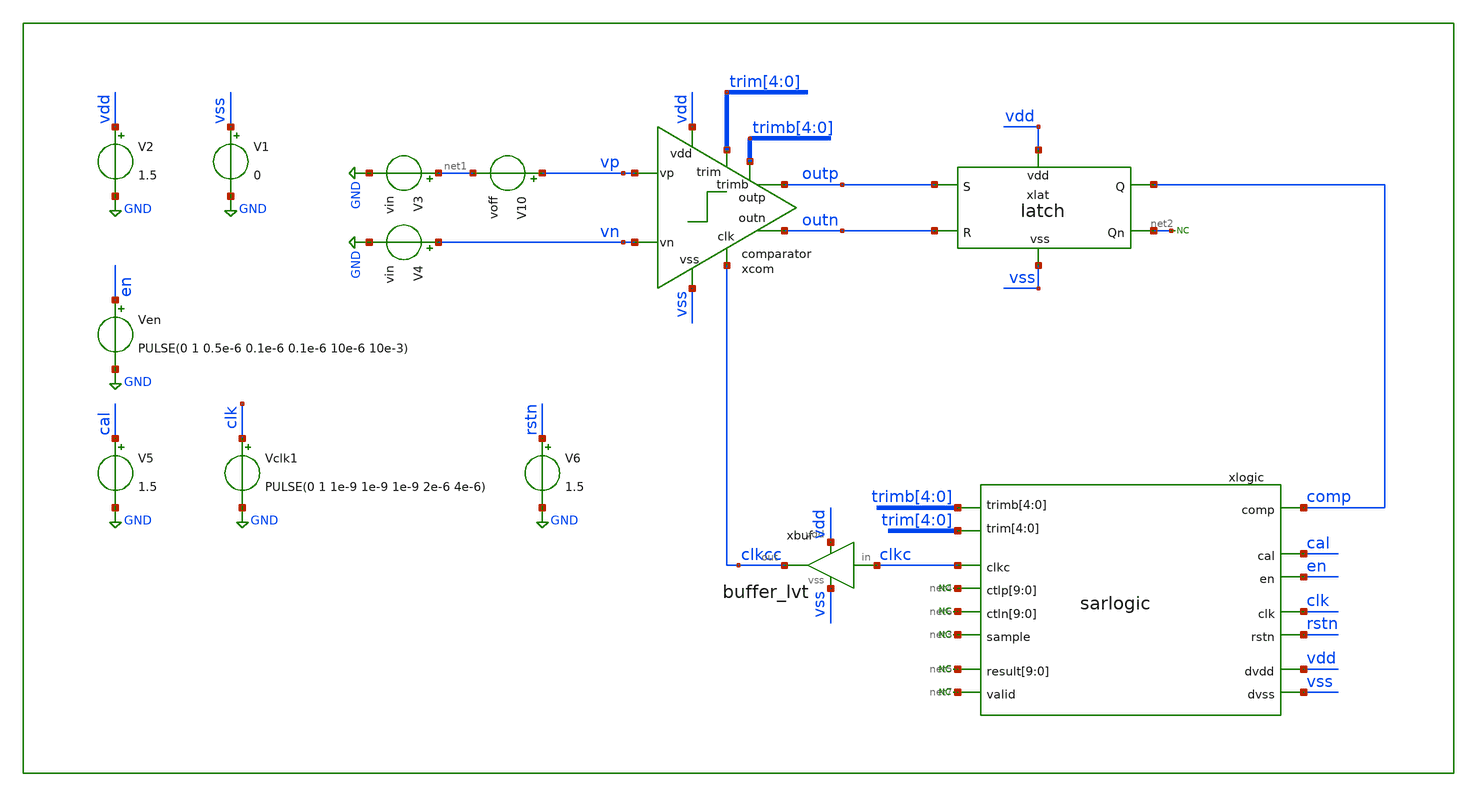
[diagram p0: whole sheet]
** sch_path: xschem/tb/comparator/tran_comparator_trim.sch
**.subckt tran_comparator_trim
xcom vss vdd clkcc outp vp outn vn trim[4] trim[3] trim[2] trim[1] trim[0] trimb[4] trimb[3]
+ trimb[2] trimb[1] trimb[0] comparator
V1 vss GND 0
V2 vdd GND 1.5
V3 net1 GND vin
V4 vn GND vin
V10 vp net1 voff
* noconn #net3
* noconn #net4
xlat vdd comp net2 vss outn outp latch
* noconn #net2
Vclk1 clk GND PULSE(0 1 1e-9 1e-9 1e-9 2e-6 4e-6)
V5 cal GND 1.5
Ven en GND PULSE(0 1 0.5e-6 0.1e-6 0.1e-6 10e-6 10e-3)
V6 rstn GND 1.5
xlogic trim[4] trim[3] trim[2] trim[1] trim[0] trimb[4] trimb[3] trimb[2] trimb[1] trimb[0] clkc
+ comp cal en net4[9] net4[8] net4[7] net4[6] net4[5] net4[4] net4[3] net4[2] net4[1] net4[0] clk net5[9]
+ net5[8] net5[7] net5[6] net5[5] net5[4] net5[3] net5[2] net5[1] net5[0] net6[9] net6[8] net6[7] net6[6]
+ net6[5] net6[4] net6[3] net6[2] net6[1] net6[0] net7 rstn net3 vdd vss sarlogic
* noconn #net6
* noconn #net5
* noconn #net7
xbuf vdd clkc clkcc vss buffer_lvt
**** begin user architecture code
 .include $::DESIGN_PATH/sar_10b/control/cmos_cells_digital.sp
.include $::DESIGN_PATH/sar_10b/control/sarlogic.sp

.param MC_SWITCH=0
.param vin=0.75
.param voff=0

.options method trap

.control
tran 100e-9 200e-6

meas tran tip_a WHEN v(xcom.ip)=1 fall=2
meas tran tin_a WHEN v(xcom.in)=1 fall=2
meas tran tip_b WHEN v(xcom.ip)=1 fall=-2
meas tran tin_b WHEN v(xcom.in)=1 fall=-2

let delta_a = abs(tip_a-tin_a)
let delta_b = abs(tip_b-tin_b)

print delta_a
print delta_b

.endc


* FET CORNERS
.include $::SKYWATER_MODELS/corners/tt.spice
*.include $::SKYWATER_MODELS/corners/ff.spice
*.include $::SKYWATER_MODELS/corners/ss.spice
*.include $::SKYWATER_MODELS/corners/sf.spice
*.include $::SKYWATER_MODELS/corners/fs.spice

* TT + R + C
*.include $::SKYWATER_MODELS/corners/tt_rmax_cmax.spice
*.include $::SKYWATER_MODELS/corners/tt_rmin_cmin.spice
*.include $::SKYWATER_MODELS/corners/tt_rmax_cmin.spice
*.include $::SKYWATER_MODELS/corners/tt_rmin_cmax.spice

* FF + R + C
*.include $::SKYWATER_MODELS/corners/ff_rmax_cmax.spice
*.include $::SKYWATER_MODELS/corners/ff_rmin_cmin.spice
*.include $::SKYWATER_MODELS/corners/ff_rmax_cmin.spice
*.include $::SKYWATER_MODELS/corners/ff_rmin_cmax.spice


* SS + R + C
*.include $::SKYWATER_MODELS/corners/ss_rmax_cmax.spice
*.include $::SKYWATER_MODELS/corners/ss_rmin_cmin.spice
*.include $::SKYWATER_MODELS/corners/ss_rmax_cmin.spice
*.include $::SKYWATER_MODELS/corners/ss_rmin_cmax.spice

* SF + R + C
*.include $::SKYWATER_MODELS/corners/sf_rmax_cmax.spice
*.include $::SKYWATER_MODELS/corners/sf_rmin_cmin.spice
*.include $::SKYWATER_MODELS/corners/sf_rmax_cmin.spice
*.include $::SKYWATER_MODELS/corners/sf_rmin_cmax.spice

* FS + R + C
*.include $::SKYWATER_MODELS/corners/fs_rmax_cmax.spice
*.include $::SKYWATER_MODELS/corners/fs_rmin_cmin.spice
*.include $::SKYWATER_MODELS/corners/fs_rmax_cmin.spice
*.include $::SKYWATER_MODELS/corners/fs_rmin_cmax.spice

**** end user architecture code
**.ends

* expanding   symbol:  sar_10b/comparator/comparator.sym # of pins=9
** sym_path: xschem/sar_10b/comparator/comparator.sym
** sch_path: xschem/sar_10b/comparator/comparator.sch
.subckt comparator vss vdd clk outp vp outn vn trim[4] trim[3] trim[2] trim[1] trim[0] trimb[4]
+ trimb[3] trimb[2] trimb[1] trimb[0]
*.ipin vn
*.ipin vp
*.ipin clk
*.iopin vdd
*.iopin vss
*.opin outp
*.opin outn
*.ipin trim[4],trim[3],trim[2],trim[1],trim[0]
*.ipin trimb[4],trimb[3],trimb[2],trimb[1],trimb[0]
XMdiff diff clk vss vss sky130_fd_pr__nfet_01v8 L=0.3 W=1 nf=1 ad='int((nf+1)/2) * W/nf * 0.29' as='int((nf+2)/2) * W/nf * 0.29'
+ pd='2*int((nf+1)/2) * (W/nf + 0.29)' ps='2*int((nf+2)/2) * (W/nf + 0.29)' nrd='0.29 / W' nrs='0.29 / W'
+ sa=0 sb=0 sd=0 mult=2 m=2
XMinn in vn diff vss sky130_fd_pr__nfet_01v8 L=0.3 W=1 nf=1 ad='int((nf+1)/2) * W/nf * 0.29' as='int((nf+2)/2) * W/nf * 0.29'
+ pd='2*int((nf+1)/2) * (W/nf + 0.29)' ps='2*int((nf+2)/2) * (W/nf + 0.29)' nrd='0.29 / W' nrs='0.29 / W'
+ sa=0 sb=0 sd=0 mult=1 m=1
XMinp ip vp diff vss sky130_fd_pr__nfet_01v8 L=0.3 W=1 nf=1 ad='int((nf+1)/2) * W/nf * 0.29' as='int((nf+2)/2) * W/nf * 0.29'
+ pd='2*int((nf+1)/2) * (W/nf + 0.29)' ps='2*int((nf+2)/2) * (W/nf + 0.29)' nrd='0.29 / W' nrs='0.29 / W'
+ sa=0 sb=0 sd=0 mult=1 m=1
XMl4 outp outn vdd vdd sky130_fd_pr__pfet_01v8 L=0.3 W=1 nf=1 ad='int((nf+1)/2) * W/nf * 0.29' as='int((nf+2)/2) * W/nf * 0.29'
+ pd='2*int((nf+1)/2) * (W/nf + 0.29)' ps='2*int((nf+2)/2) * (W/nf + 0.29)' nrd='0.29 / W' nrs='0.29 / W'
+ sa=0 sb=0 sd=0 mult=1 m=1
XMl3 outn outp vdd vdd sky130_fd_pr__pfet_01v8 L=0.3 W=1 nf=1 ad='int((nf+1)/2) * W/nf * 0.29' as='int((nf+2)/2) * W/nf * 0.29'
+ pd='2*int((nf+1)/2) * (W/nf + 0.29)' ps='2*int((nf+2)/2) * (W/nf + 0.29)' nrd='0.29 / W' nrs='0.29 / W'
+ sa=0 sb=0 sd=0 mult=1 m=1
XM3 outp clk vdd vdd sky130_fd_pr__pfet_01v8 L=0.3 W=1 nf=1 ad='int((nf+1)/2) * W/nf * 0.29' as='int((nf+2)/2) * W/nf * 0.29'
+ pd='2*int((nf+1)/2) * (W/nf + 0.29)' ps='2*int((nf+2)/2) * (W/nf + 0.29)' nrd='0.29 / W' nrs='0.29 / W'
+ sa=0 sb=0 sd=0 mult=1 m=1
XM2 outn clk vdd vdd sky130_fd_pr__pfet_01v8 L=0.3 W=1 nf=1 ad='int((nf+1)/2) * W/nf * 0.29' as='int((nf+2)/2) * W/nf * 0.29'
+ pd='2*int((nf+1)/2) * (W/nf + 0.29)' ps='2*int((nf+2)/2) * (W/nf + 0.29)' nrd='0.29 / W' nrs='0.29 / W'
+ sa=0 sb=0 sd=0 mult=1 m=1
XMl1 outn outp in vss sky130_fd_pr__nfet_01v8 L=0.3 W=1 nf=1 ad='int((nf+1)/2) * W/nf * 0.29' as='int((nf+2)/2) * W/nf * 0.29'
+ pd='2*int((nf+1)/2) * (W/nf + 0.29)' ps='2*int((nf+2)/2) * (W/nf + 0.29)' nrd='0.29 / W' nrs='0.29 / W'
+ sa=0 sb=0 sd=0 mult=1 m=1
XMl2 outp outn ip vss sky130_fd_pr__nfet_01v8 L=0.3 W=1 nf=1 ad='int((nf+1)/2) * W/nf * 0.29' as='int((nf+2)/2) * W/nf * 0.29'
+ pd='2*int((nf+1)/2) * (W/nf + 0.29)' ps='2*int((nf+2)/2) * (W/nf + 0.29)' nrd='0.29 / W' nrs='0.29 / W'
+ sa=0 sb=0 sd=0 mult=1 m=1
XM4 ip clk vdd vdd sky130_fd_pr__pfet_01v8 L=0.3 W=1 nf=1 ad='int((nf+1)/2) * W/nf * 0.29' as='int((nf+2)/2) * W/nf * 0.29'
+ pd='2*int((nf+1)/2) * (W/nf + 0.29)' ps='2*int((nf+2)/2) * (W/nf + 0.29)' nrd='0.29 / W' nrs='0.29 / W'
+ sa=0 sb=0 sd=0 mult=1 m=1
XM1 in clk vdd vdd sky130_fd_pr__pfet_01v8 L=0.3 W=1 nf=1 ad='int((nf+1)/2) * W/nf * 0.29' as='int((nf+2)/2) * W/nf * 0.29'
+ pd='2*int((nf+1)/2) * (W/nf + 0.29)' ps='2*int((nf+2)/2) * (W/nf + 0.29)' nrd='0.29 / W' nrs='0.29 / W'
+ sa=0 sb=0 sd=0 mult=1 m=1
x2 in trim[4] trim[3] trim[2] trim[1] trim[0] vss trim
x3 ip trimb[4] trimb[3] trimb[2] trimb[1] trimb[0] vss trim
.ends


* expanding   symbol:  sar_10b/latch/latch.sym # of pins=6
** sym_path: xschem/sar_10b/latch/latch.sym
** sch_path: xschem/sar_10b/latch/latch.sch
.subckt latch vdd Q Qn vss R S
*.ipin S
*.ipin R
*.iopin vss
*.iopin vdd
*.opin Q
*.opin Qn
x1 vdd Qn Q vss inv_lvt
x2 vdd Q Qn vss inv_lvt
x3 vdd R net2 vss inv_lvt
x4 vdd S net1 vss inv_lvt
XM3 Qn net1 vss vss sky130_fd_pr__nfet_01v8_lvt L=0.4 W=1 nf=1 ad='int((nf+1)/2) * W/nf * 0.29' as='int((nf+2)/2) * W/nf * 0.29'
+ pd='2*int((nf+1)/2) * (W/nf + 0.29)' ps='2*int((nf+2)/2) * (W/nf + 0.29)' nrd='0.29 / W' nrs='0.29 / W'
+ sa=0 sb=0 sd=0 mult=1 m=1
XM1 Q net2 vss vss sky130_fd_pr__nfet_01v8_lvt L=0.4 W=1 nf=1 ad='int((nf+1)/2) * W/nf * 0.29' as='int((nf+2)/2) * W/nf * 0.29'
+ pd='2*int((nf+1)/2) * (W/nf + 0.29)' ps='2*int((nf+2)/2) * (W/nf + 0.29)' nrd='0.29 / W' nrs='0.29 / W'
+ sa=0 sb=0 sd=0 mult=1 m=1
.ends


* expanding   symbol:  sar_10b/control/sarlogic.sym # of pins=15
** sym_path: xschem/sar_10b/control/sarlogic.sym
** sch_path: xschem/sar_10b/control/sarlogic.sch
.subckt sarlogic trim[4] trim[3] trim[2] trim[1] trim[0] trimb[4] trimb[3] trimb[2] trimb[1]
+ trimb[0] clkc comp cal en ctlp[9] ctlp[8] ctlp[7] ctlp[6] ctlp[5] ctlp[4] ctlp[3] ctlp[2] ctlp[1] ctlp[0]
+ clk result[9] result[8] result[7] result[6] result[5] result[4] result[3] result[2] result[1] result[0]
+ ctln[9] ctln[8] ctln[7] ctln[6] ctln[5] ctln[4] ctln[3] ctln[2] ctln[1] ctln[0] valid rstn sample dvdd dvss
*.opin clkc
*.opin ctlp[9],ctlp[8],ctlp[7],ctlp[6],ctlp[5],ctlp[4],ctlp[3],ctlp[2],ctlp[1],ctlp[0]
*.opin ctln[9],ctln[8],ctln[7],ctln[6],ctln[5],ctln[4],ctln[3],ctln[2],ctln[1],ctln[0]
*.opin sample
*.opin trim[4],trim[3],trim[2],trim[1],trim[0]
*.opin trimb[4],trimb[3],trimb[2],trimb[1],trimb[0]
*.ipin comp
*.ipin cal
*.ipin en
*.ipin clk
*.ipin
*+ result[9],result[8],result[7],result[6],result[5],result[4],result[3],result[2],result[1],result[0]
*.ipin valid
*.ipin rstn
*.iopin dvdd
*.iopin dvss
* noconn comp
* noconn ctlp[9:0]
* noconn ctln[9:0]
* noconn sample
* noconn trimb[4:0]
* noconn trim[4:0]
* noconn result[9:0]
* noconn valid
* noconn clkc
* noconn clk
* noconn en
* noconn cal
* noconn rstn
**** begin user architecture code
.include $::DESIGN_PATH/sar_10b/control/cmos_cells_digital.sp
.include $::DESIGN_PATH/sar_10b/control/sarlogic.sp

**** end user architecture code
* noconn dvdd
* noconn dvss
**** begin user architecture code
* Keep the sar_logic underscore name. Otherwise xschem gets confused.
Xuut dclk drstn den dcomp dcal dvalid dres0 dres1 dres2 dres3 dres4 dres5 dres6 dres7 dres8 dres9
+ dsamp dctlp0 dctlp1 dctlp2 dctlp3 dctlp4 dctlp5 dctlp6 dctlp7 dctlp8 dctlp9 dctln0 dctln1 dctln2 dctln3
+ dctln4 dctln5 dctln6 dctln7 dctln8 dctln9 dtrim0 dtrim1 dtrim2 dtrim3 dtrim4 dtrimb0 dtrimb1 dtrimb2
+ dtrimb3 dtrimb4 dclkc sar_logic

.model adc_buff adc_bridge(in_low = 0.2 in_high=0.8)
.model dac_buff dac_bridge(out_high = 1.2)

Aad [clk rstn en comp cal] [dclk drstn den dcomp dcal] adc_buff
Ada1 [dctlp0 dctlp1 dctlp2 dctlp3 dctlp4 dctlp5 dctlp6 dctlp7 dctlp8 dctlp9] [ctlp_0_ ctlp_1_
+ ctlp_2_ ctlp_3_ ctlp_4_ ctlp_5_ ctlp_6_ ctlp_7_ ctlp_8_ ctlp_9_] dac_buff
Ada2 [dctln0 dctln1 dctln2 dctln3 dctln4 dctln5 dctln6 dctln7 dctln8 dctln9] [ctln_0_ ctln_1_
+ ctln_2_ ctln_3_ ctln_4_ ctln_5_ ctln_6_ ctln_7_ ctln_8_ ctln_9_] dac_buff
Ada3 [dres0 dres1 dres2 dres3 dres4 dres5 dres6 dres7 dres8 dres9 dsamp dclkc] [res0 res1 res2 res3
+ res4 res5 res6 res7 res8 res9 sample clkc] dac_buff
Ada4 [dtrim4 dtrim3 dtrim2 dtrim1 dtrim0 dtrimb4 dtrimb3 dtrimb2 dtrimb1 dtrimb0] [trim_4_ trim_3_
+ trim_2_ trim_1_ trim_0_ trimb_4_ trimb_3_ trimb_2_ trimb_1_ trimb_0_ ] dac_buff

**** end user architecture code
.ends


* expanding   symbol:  logic/buffer_lvt.sym # of pins=4
** sym_path: xschem/logic/buffer_lvt.sym
** sch_path: xschem/logic/buffer_lvt.sch
.subckt buffer_lvt vdd in out vss
*.iopin vdd
*.iopin vss
*.ipin in
*.opin out
XM1 net1 in vss vss sky130_fd_pr__nfet_01v8_lvt L=0.4 W=1 nf=1 ad='int((nf+1)/2) * W/nf * 0.29' as='int((nf+2)/2) * W/nf * 0.29'
+ pd='2*int((nf+1)/2) * (W/nf + 0.29)' ps='2*int((nf+2)/2) * (W/nf + 0.29)' nrd='0.29 / W' nrs='0.29 / W'
+ sa=0 sb=0 sd=0 mult=1 m=1
XM2 net1 in vdd vdd sky130_fd_pr__pfet_01v8_lvt L=0.4 W=1 nf=1 ad='int((nf+1)/2) * W/nf * 0.29' as='int((nf+2)/2) * W/nf * 0.29'
+ pd='2*int((nf+1)/2) * (W/nf + 0.29)' ps='2*int((nf+2)/2) * (W/nf + 0.29)' nrd='0.29 / W' nrs='0.29 / W'
+ sa=0 sb=0 sd=0 mult=1 m=1
XM3 out net1 vss vss sky130_fd_pr__nfet_01v8_lvt L=0.4 W=1 nf=1 ad='int((nf+1)/2) * W/nf * 0.29' as='int((nf+2)/2) * W/nf * 0.29'
+ pd='2*int((nf+1)/2) * (W/nf + 0.29)' ps='2*int((nf+2)/2) * (W/nf + 0.29)' nrd='0.29 / W' nrs='0.29 / W'
+ sa=0 sb=0 sd=0 mult=1 m=1
XM4 out net1 vdd vdd sky130_fd_pr__pfet_01v8_lvt L=0.4 W=1 nf=1 ad='int((nf+1)/2) * W/nf * 0.29' as='int((nf+2)/2) * W/nf * 0.29'
+ pd='2*int((nf+1)/2) * (W/nf + 0.29)' ps='2*int((nf+2)/2) * (W/nf + 0.29)' nrd='0.29 / W' nrs='0.29 / W'
+ sa=0 sb=0 sd=0 mult=1 m=1
.ends


* expanding   symbol:  sar_10b/comparator/trim.sym # of pins=3
** sym_path: xschem/sar_10b/comparator/trim.sym
** sch_path: xschem/sar_10b/comparator/trim.sch
.subckt trim drain d[4] d[3] d[2] d[1] d[0] vss
*.iopin vss
*.ipin d[4],d[3],d[2],d[1],d[0]
*.opin drain
XM4[7] n4 d[4] vss vss sky130_fd_pr__nfet_01v8_lvt L=0.3 W=1 nf=1 ad='int((nf+1)/2) * W/nf * 0.29' as='int((nf+2)/2) * W/nf * 0.29'
+ pd='2*int((nf+1)/2) * (W/nf + 0.29)' ps='2*int((nf+2)/2) * (W/nf + 0.29)' nrd='0.29 / W' nrs='0.29 / W'
+ sa=0 sb=0 sd=0 mult=1 m=1
XM4[6] n4 d[4] vss vss sky130_fd_pr__nfet_01v8_lvt L=0.3 W=1 nf=1 ad='int((nf+1)/2) * W/nf * 0.29' as='int((nf+2)/2) * W/nf * 0.29'
+ pd='2*int((nf+1)/2) * (W/nf + 0.29)' ps='2*int((nf+2)/2) * (W/nf + 0.29)' nrd='0.29 / W' nrs='0.29 / W'
+ sa=0 sb=0 sd=0 mult=1 m=1
XM4[5] n4 d[4] vss vss sky130_fd_pr__nfet_01v8_lvt L=0.3 W=1 nf=1 ad='int((nf+1)/2) * W/nf * 0.29' as='int((nf+2)/2) * W/nf * 0.29'
+ pd='2*int((nf+1)/2) * (W/nf + 0.29)' ps='2*int((nf+2)/2) * (W/nf + 0.29)' nrd='0.29 / W' nrs='0.29 / W'
+ sa=0 sb=0 sd=0 mult=1 m=1
XM4[4] n4 d[4] vss vss sky130_fd_pr__nfet_01v8_lvt L=0.3 W=1 nf=1 ad='int((nf+1)/2) * W/nf * 0.29' as='int((nf+2)/2) * W/nf * 0.29'
+ pd='2*int((nf+1)/2) * (W/nf + 0.29)' ps='2*int((nf+2)/2) * (W/nf + 0.29)' nrd='0.29 / W' nrs='0.29 / W'
+ sa=0 sb=0 sd=0 mult=1 m=1
XM4[3] n4 d[4] vss vss sky130_fd_pr__nfet_01v8_lvt L=0.3 W=1 nf=1 ad='int((nf+1)/2) * W/nf * 0.29' as='int((nf+2)/2) * W/nf * 0.29'
+ pd='2*int((nf+1)/2) * (W/nf + 0.29)' ps='2*int((nf+2)/2) * (W/nf + 0.29)' nrd='0.29 / W' nrs='0.29 / W'
+ sa=0 sb=0 sd=0 mult=1 m=1
XM4[2] n4 d[4] vss vss sky130_fd_pr__nfet_01v8_lvt L=0.3 W=1 nf=1 ad='int((nf+1)/2) * W/nf * 0.29' as='int((nf+2)/2) * W/nf * 0.29'
+ pd='2*int((nf+1)/2) * (W/nf + 0.29)' ps='2*int((nf+2)/2) * (W/nf + 0.29)' nrd='0.29 / W' nrs='0.29 / W'
+ sa=0 sb=0 sd=0 mult=1 m=1
XM4[1] n4 d[4] vss vss sky130_fd_pr__nfet_01v8_lvt L=0.3 W=1 nf=1 ad='int((nf+1)/2) * W/nf * 0.29' as='int((nf+2)/2) * W/nf * 0.29'
+ pd='2*int((nf+1)/2) * (W/nf + 0.29)' ps='2*int((nf+2)/2) * (W/nf + 0.29)' nrd='0.29 / W' nrs='0.29 / W'
+ sa=0 sb=0 sd=0 mult=1 m=1
XM4[0] n4 d[4] vss vss sky130_fd_pr__nfet_01v8_lvt L=0.3 W=1 nf=1 ad='int((nf+1)/2) * W/nf * 0.29' as='int((nf+2)/2) * W/nf * 0.29'
+ pd='2*int((nf+1)/2) * (W/nf + 0.29)' ps='2*int((nf+2)/2) * (W/nf + 0.29)' nrd='0.29 / W' nrs='0.29 / W'
+ sa=0 sb=0 sd=0 mult=1 m=1
XM3[3] n3 d[3] vss vss sky130_fd_pr__nfet_01v8_lvt L=0.3 W=1 nf=1 ad='int((nf+1)/2) * W/nf * 0.29' as='int((nf+2)/2) * W/nf * 0.29'
+ pd='2*int((nf+1)/2) * (W/nf + 0.29)' ps='2*int((nf+2)/2) * (W/nf + 0.29)' nrd='0.29 / W' nrs='0.29 / W'
+ sa=0 sb=0 sd=0 mult=1 m=1
XM3[2] n3 d[3] vss vss sky130_fd_pr__nfet_01v8_lvt L=0.3 W=1 nf=1 ad='int((nf+1)/2) * W/nf * 0.29' as='int((nf+2)/2) * W/nf * 0.29'
+ pd='2*int((nf+1)/2) * (W/nf + 0.29)' ps='2*int((nf+2)/2) * (W/nf + 0.29)' nrd='0.29 / W' nrs='0.29 / W'
+ sa=0 sb=0 sd=0 mult=1 m=1
XM3[1] n3 d[3] vss vss sky130_fd_pr__nfet_01v8_lvt L=0.3 W=1 nf=1 ad='int((nf+1)/2) * W/nf * 0.29' as='int((nf+2)/2) * W/nf * 0.29'
+ pd='2*int((nf+1)/2) * (W/nf + 0.29)' ps='2*int((nf+2)/2) * (W/nf + 0.29)' nrd='0.29 / W' nrs='0.29 / W'
+ sa=0 sb=0 sd=0 mult=1 m=1
XM3[0] n3 d[3] vss vss sky130_fd_pr__nfet_01v8_lvt L=0.3 W=1 nf=1 ad='int((nf+1)/2) * W/nf * 0.29' as='int((nf+2)/2) * W/nf * 0.29'
+ pd='2*int((nf+1)/2) * (W/nf + 0.29)' ps='2*int((nf+2)/2) * (W/nf + 0.29)' nrd='0.29 / W' nrs='0.29 / W'
+ sa=0 sb=0 sd=0 mult=1 m=1
XM2[1] n2 d[2] vss vss sky130_fd_pr__nfet_01v8_lvt L=0.3 W=1 nf=1 ad='int((nf+1)/2) * W/nf * 0.29' as='int((nf+2)/2) * W/nf * 0.29'
+ pd='2*int((nf+1)/2) * (W/nf + 0.29)' ps='2*int((nf+2)/2) * (W/nf + 0.29)' nrd='0.29 / W' nrs='0.29 / W'
+ sa=0 sb=0 sd=0 mult=1 m=1
XM2[0] n2 d[2] vss vss sky130_fd_pr__nfet_01v8_lvt L=0.3 W=1 nf=1 ad='int((nf+1)/2) * W/nf * 0.29' as='int((nf+2)/2) * W/nf * 0.29'
+ pd='2*int((nf+1)/2) * (W/nf + 0.29)' ps='2*int((nf+2)/2) * (W/nf + 0.29)' nrd='0.29 / W' nrs='0.29 / W'
+ sa=0 sb=0 sd=0 mult=1 m=1
XM1 n1 d[1] vss vss sky130_fd_pr__nfet_01v8_lvt L=0.3 W=1 nf=1 ad='int((nf+1)/2) * W/nf * 0.29' as='int((nf+2)/2) * W/nf * 0.29'
+ pd='2*int((nf+1)/2) * (W/nf + 0.29)' ps='2*int((nf+2)/2) * (W/nf + 0.29)' nrd='0.29 / W' nrs='0.29 / W'
+ sa=0 sb=0 sd=0 mult=1 m=1
XM0 n0 d[0] vss vss sky130_fd_pr__nfet_01v8_lvt L=0.3 W=1 nf=1 ad='int((nf+1)/2) * W/nf * 0.29' as='int((nf+2)/2) * W/nf * 0.29'
+ pd='2*int((nf+1)/2) * (W/nf + 0.29)' ps='2*int((nf+2)/2) * (W/nf + 0.29)' nrd='0.29 / W' nrs='0.29 / W'
+ sa=0 sb=0 sd=0 mult=1 m=1
x4[7] drain n4 trimcap
x4[6] drain n4 trimcap
x4[5] drain n4 trimcap
x4[4] drain n4 trimcap
x4[3] drain n4 trimcap
x4[2] drain n4 trimcap
x4[1] drain n4 trimcap
x4[0] drain n4 trimcap
x3[3] drain n3 trimcap
x3[2] drain n3 trimcap
x3[1] drain n3 trimcap
x3[0] drain n3 trimcap
x2[1] drain n2 trimcap
x2[0] drain n2 trimcap
x1 drain n1 trimcap
x0 drain n0 trimcap
.ends


* expanding   symbol:  logic/inv_lvt.sym # of pins=4
** sym_path: xschem/logic/inv_lvt.sym
** sch_path: xschem/logic/inv_lvt.sch
.subckt inv_lvt vdd in out vss
*.iopin vdd
*.iopin vss
*.ipin in
*.opin out
XM1 out in vss vss sky130_fd_pr__nfet_01v8_lvt L=0.4 W=1 nf=1 ad='int((nf+1)/2) * W/nf * 0.29' as='int((nf+2)/2) * W/nf * 0.29'
+ pd='2*int((nf+1)/2) * (W/nf + 0.29)' ps='2*int((nf+2)/2) * (W/nf + 0.29)' nrd='0.29 / W' nrs='0.29 / W'
+ sa=0 sb=0 sd=0 mult=1 m=1
XM2 out in vdd vdd sky130_fd_pr__pfet_01v8_lvt L=0.4 W=1 nf=1 ad='int((nf+1)/2) * W/nf * 0.29' as='int((nf+2)/2) * W/nf * 0.29'
+ pd='2*int((nf+1)/2) * (W/nf + 0.29)' ps='2*int((nf+2)/2) * (W/nf + 0.29)' nrd='0.29 / W' nrs='0.29 / W'
+ sa=0 sb=0 sd=0 mult=1 m=1
.ends


* expanding   symbol:  sar_10b/comparator/trimcap.sym # of pins=2
** sym_path: xschem/sar_10b/comparator/trimcap.sym
** sch_path: xschem/sar_10b/comparator/trimcap.sch
.subckt trimcap cp cn
*.iopin cp
*.iopin cn
c0 net1 cn 2f m=1
c1 cp net1 1f m=1
.ends

.GLOBAL GND
.end
